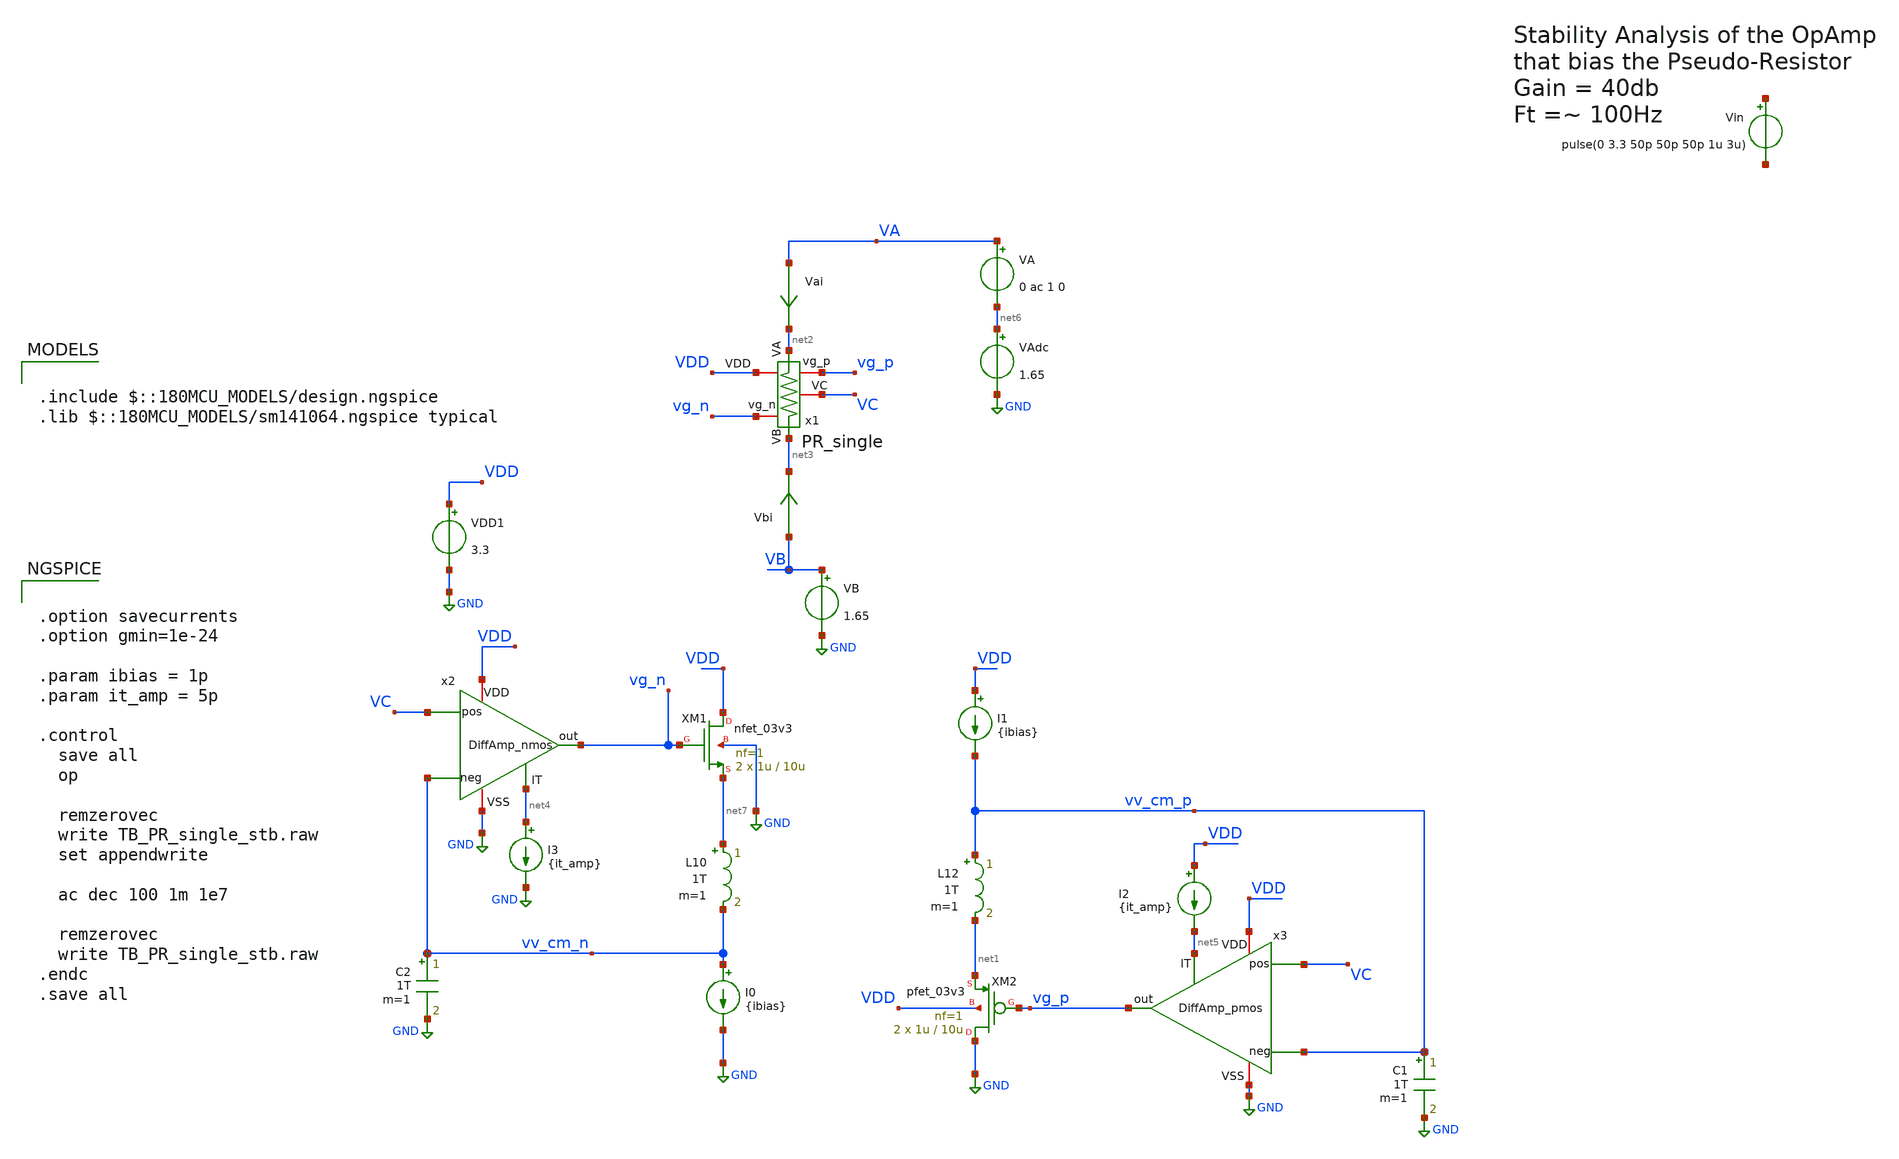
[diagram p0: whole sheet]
** sch_path: TIA/xschem/pseudo_res_dir/TB_PR_single_stb.sch
**.subckt TB_PR_single_stb
x1 VDD net2 vg_p VC vg_n net3 PR_single
XM1 VDD vg_n net7 GND nfet_03v3 L=10u W=1u nf=1 ad='int((nf+1)/2) * W/nf * 0.18u' as='int((nf+2)/2) * W/nf * 0.18u'
+ pd='2*int((nf+1)/2) * (W/nf + 0.18u)' ps='2*int((nf+2)/2) * (W/nf + 0.18u)' nrd='0.18u / W' nrs='0.18u / W'
+ sa=0 sb=0 sd=0 m=2
XM2 GND vg_p net1 VDD pfet_03v3 L=10u W=1u nf=1 ad='int((nf+1)/2) * W/nf * 0.18u' as='int((nf+2)/2) * W/nf * 0.18u'
+ pd='2*int((nf+1)/2) * (W/nf + 0.18u)' ps='2*int((nf+2)/2) * (W/nf + 0.18u)' nrd='0.18u / W' nrs='0.18u / W'
+ sa=0 sb=0 sd=0 m=2
I0 vv_cm_n GND {ibias}
I1 VDD vv_cm_p {ibias}
VDD1 VDD GND 3.3
Vai VA net2 0
.save i(vai)
Vbi VB net3 0
.save i(vbi)
x2 VDD GND VC vv_cm_n net4 vg_n DiffAmp_nmos
I2 VDD net5 {it_amp}
x3 VDD GND net5 vv_cm_p VC vg_p DiffAmp_pmos
I3 net4 GND {it_amp}
VA VA net6 0 ac 1 0
VB VB GND 1.65
VAdc net6 GND 1.65
C1 vv_cm_p GND 1T m=1
L12 vv_cm_p net1 1T m=1
C2 vv_cm_n GND 1T m=1
L10 net7 vv_cm_n 1T m=1
**** begin user architecture code

.include $::180MCU_MODELS/design.ngspice
.lib $::180MCU_MODELS/sm141064.ngspice typical



.option savecurrents
.option gmin=1e-24

.param ibias = 1p
.param it_amp = 5p

.control
  save all
  op

  remzerovec
  write TB_PR_single_stb.raw
  set appendwrite

  ac dec 100 1m 1e7

  remzerovec
  write TB_PR_single_stb.raw
.endc
.save all


**** end user architecture code
**.ends
.GLOBAL GND
.end
